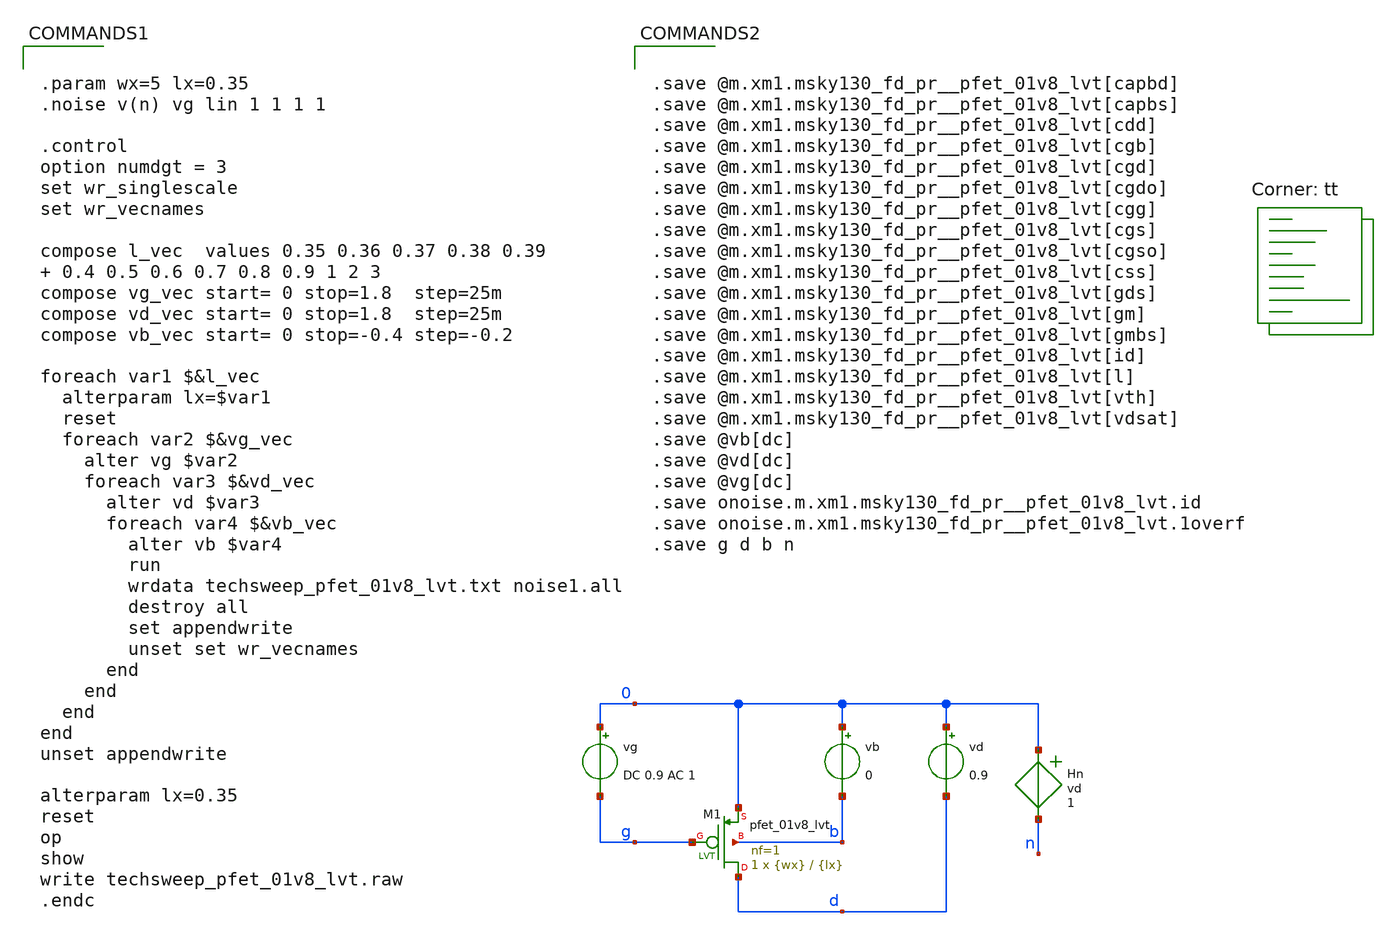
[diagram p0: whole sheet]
** sch_path: gmID-Design/Extraction/sky130A/techsweep_pfet_01v8_lvt.sch
**.subckt techsweep_pfet_01v8_lvt
Hn 0 n vd 1
vg 0 g DC 0.9 AC 1
vd 0 d 0.9
XM1 d g 0 b sky130_fd_pr__pfet_01v8_lvt L={lx} W={wx} nf=1 ad='int((nf+1)/2) * W/nf * 0.29' as='int((nf+2)/2) * W/nf * 0.29'
+ pd='2*int((nf+1)/2) * (W/nf + 0.29)' ps='2*int((nf+2)/2) * (W/nf + 0.29)' nrd='0.29 / W' nrs='0.29 / W'
+ sa=0 sb=0 sd=0 mult=1 m=1
vb 0 b 0
**** begin user architecture code


.param wx=5 lx=0.35
.noise v(n) vg lin 1 1 1 1

.control
option numdgt = 3
set wr_singlescale
set wr_vecnames

compose l_vec  values 0.35 0.36 0.37 0.38 0.39  0.4 0.5 0.6 0.7 0.8 0.9 1 2 3
compose vg_vec start= 0 stop=1.8  step=25m
compose vd_vec start= 0 stop=1.8  step=25m
compose vb_vec start= 0 stop=-0.4 step=-0.2

foreach var1 $&l_vec
  alterparam lx=$var1
  reset
  foreach var2 $&vg_vec
    alter vg $var2
    foreach var3 $&vd_vec
      alter vd $var3
      foreach var4 $&vb_vec
        alter vb $var4
        run
        wrdata techsweep_pfet_01v8_lvt.txt noise1.all
        destroy all
        set appendwrite
        unset set wr_vecnames
      end
    end
  end
end
unset appendwrite

alterparam lx=0.35
reset
op
show
write techsweep_pfet_01v8_lvt.raw
.endc


.lib $::SKYWATER_MODELS/sky130.lib.spice tt


.save @m.xm1.msky130_fd_pr__pfet_01v8_lvt[capbd]
.save @m.xm1.msky130_fd_pr__pfet_01v8_lvt[capbs]
.save @m.xm1.msky130_fd_pr__pfet_01v8_lvt[cdd]
.save @m.xm1.msky130_fd_pr__pfet_01v8_lvt[cgb]
.save @m.xm1.msky130_fd_pr__pfet_01v8_lvt[cgd]
.save @m.xm1.msky130_fd_pr__pfet_01v8_lvt[cgdo]
.save @m.xm1.msky130_fd_pr__pfet_01v8_lvt[cgg]
.save @m.xm1.msky130_fd_pr__pfet_01v8_lvt[cgs]
.save @m.xm1.msky130_fd_pr__pfet_01v8_lvt[cgso]
.save @m.xm1.msky130_fd_pr__pfet_01v8_lvt[css]
.save @m.xm1.msky130_fd_pr__pfet_01v8_lvt[gds]
.save @m.xm1.msky130_fd_pr__pfet_01v8_lvt[gm]
.save @m.xm1.msky130_fd_pr__pfet_01v8_lvt[gmbs]
.save @m.xm1.msky130_fd_pr__pfet_01v8_lvt[id]
.save @m.xm1.msky130_fd_pr__pfet_01v8_lvt[l]
.save @m.xm1.msky130_fd_pr__pfet_01v8_lvt[vth]
.save @m.xm1.msky130_fd_pr__pfet_01v8_lvt[vdsat]
.save @vb[dc]
.save @vd[dc]
.save @vg[dc]
.save onoise.m.xm1.msky130_fd_pr__pfet_01v8_lvt.id
.save onoise.m.xm1.msky130_fd_pr__pfet_01v8_lvt.1overf
.save g d b n


**** end user architecture code
**.ends
.end
